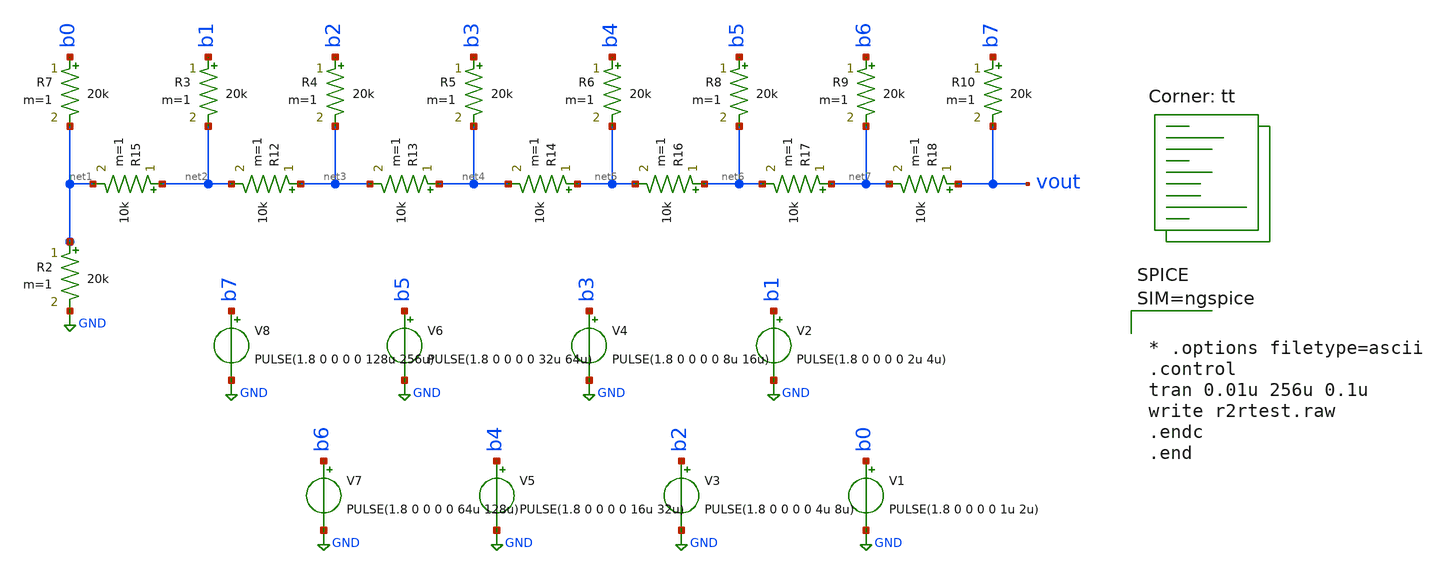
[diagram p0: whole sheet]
** sch_path: xschem/r2r-dac.sch
**.subckt r2r-dac
R2 net1 GND 20k m=1
R7 b0 net1 20k m=1
R3 b1 net2 20k m=1
R4 b2 net3 20k m=1
R5 b3 net4 20k m=1
R6 b4 net5 20k m=1
R8 b5 net6 20k m=1
R9 b6 net7 20k m=1
R10 b7 vout 20k m=1
R12 net3 net2 10k m=1
R13 net4 net3 10k m=1
R14 net5 net4 10k m=1
R15 net2 net1 10k m=1
R16 net6 net5 10k m=1
R17 net7 net6 10k m=1
R18 vout net7 10k m=1
V1 b0 GND PULSE(1.8 0 0 0 0 1u 2u)
V2 b1 GND PULSE(1.8 0 0 0 0 2u 4u)
V3 b2 GND PULSE(1.8 0 0 0 0 4u 8u)
V4 b3 GND PULSE(1.8 0 0 0 0 8u 16u)
V5 b4 GND PULSE(1.8 0 0 0 0 16u 32u)
V6 b5 GND PULSE(1.8 0 0 0 0 32u 64u)
V7 b6 GND PULSE(1.8 0 0 0 0 64u 128u)
V8 b7 GND PULSE(1.8 0 0 0 0 128u 256u)
**** begin user architecture code
.lib $::SKYWATER_MODELS/sky130.lib.spice tt



* .options filetype=ascii
.control
tran 0.01u 256u 0.1u
write r2rtest.raw
.endc
.end



**** end user architecture code
**.ends
.GLOBAL GND
.end
